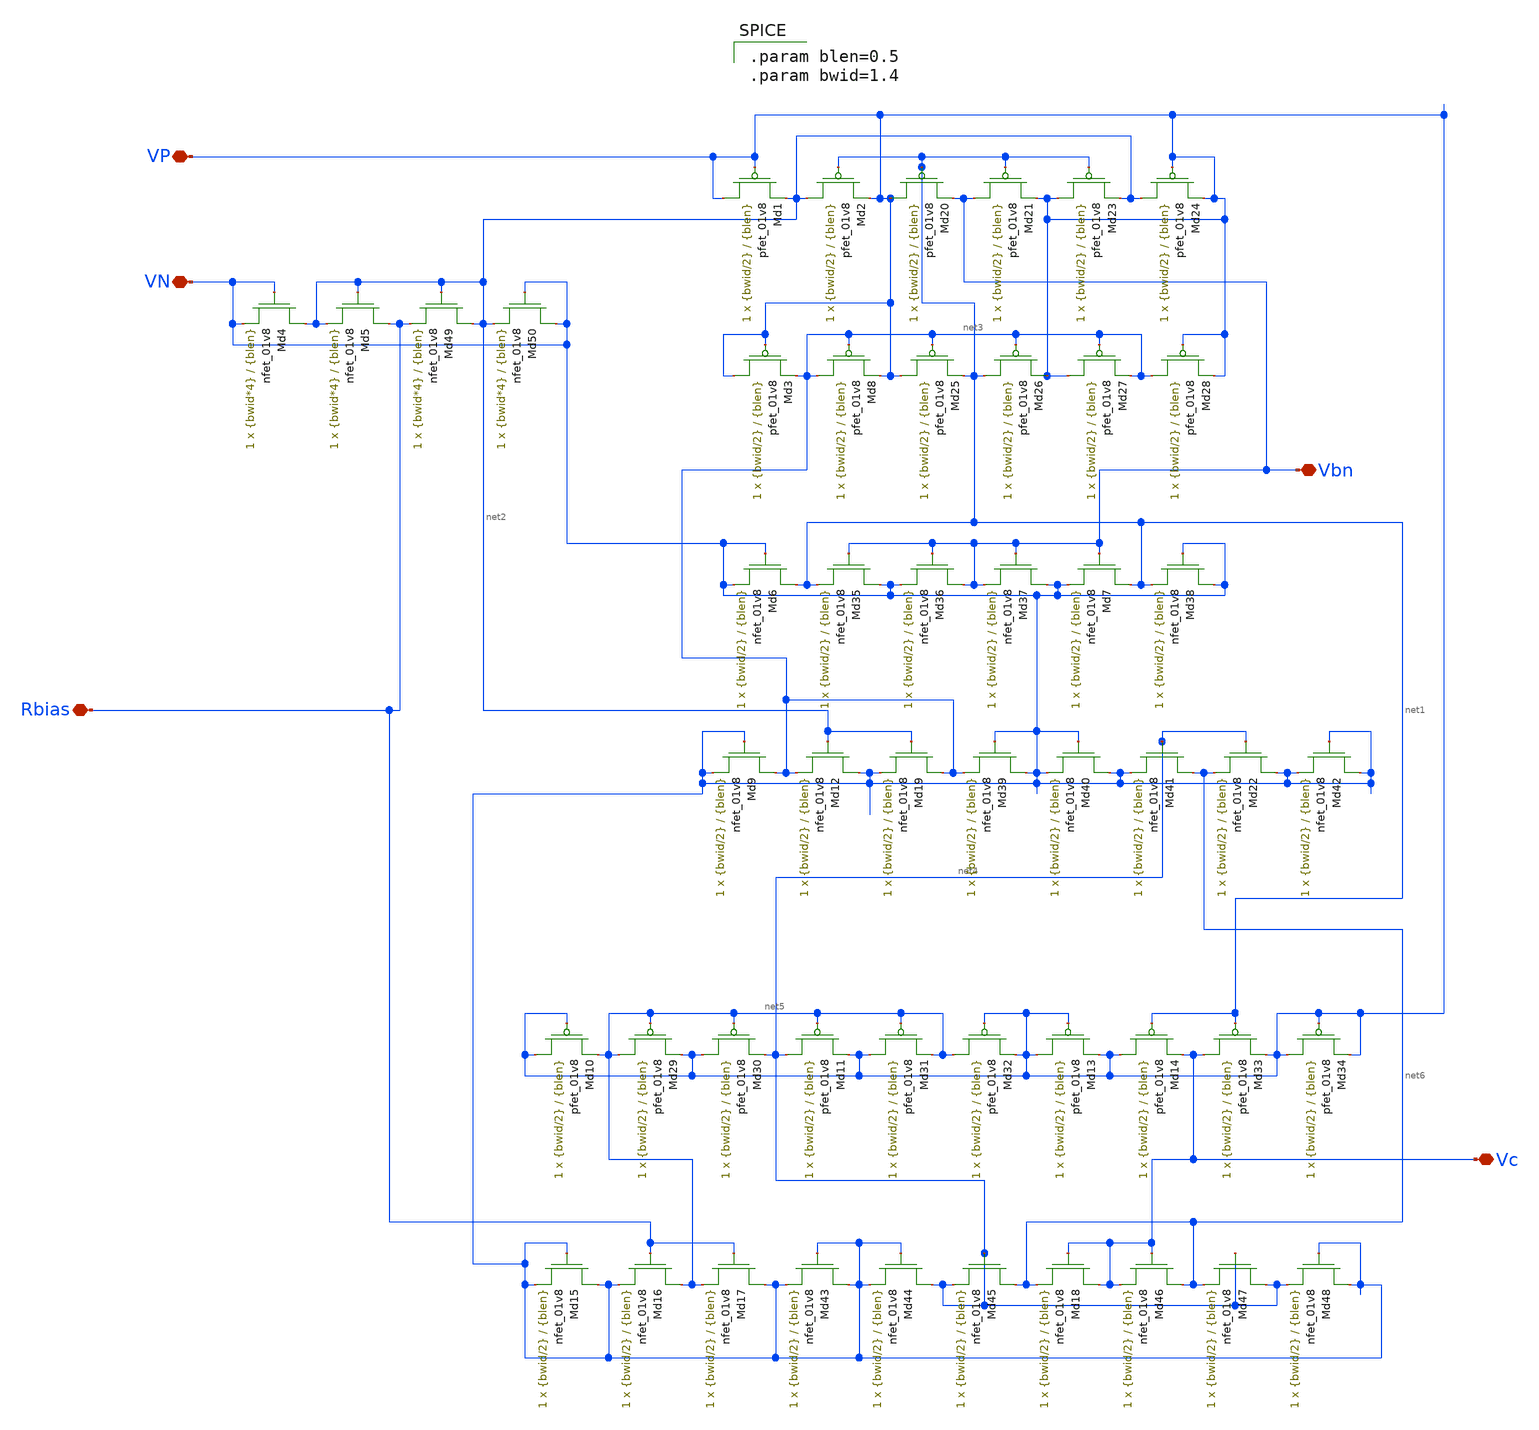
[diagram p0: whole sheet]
** sch_path: design-files/opt/biasgen_opt.sch
**.subckt biasgen_opt Rbias Vbn Vc VP VN
*.iopin Rbias
*.iopin Vbn
*.iopin Vc
*.iopin VP
*.iopin VN
XMd1 VP VP net2 VDD sky130_fd_pr__pfet_01v8 L={blen} W={bwid/2} nf=1 ad='int((nf+1)/2) * W/nf * 0.29'
+ as='int((nf+2)/2) * W/nf * 0.29' pd='2*int((nf+1)/2) * (W/nf + 0.29)' ps='2*int((nf+2)/2) * (W/nf + 0.29)'
+ nrd='0.29 / W' nrs='0.29 / W' sa=0 sb=0 sd=0 mult=1 m=1
XMd6 net1 VN VN GND sky130_fd_pr__nfet_01v8 L={blen} W={bwid/2} nf=1 ad='int((nf+1)/2) * W/nf * 0.29'
+ as='int((nf+2)/2) * W/nf * 0.29' pd='2*int((nf+1)/2) * (W/nf + 0.29)' ps='2*int((nf+2)/2) * (W/nf + 0.29)'
+ nrd='0.29 / W' nrs='0.29 / W' sa=0 sb=0 sd=0 mult=1 m=1
XMd2 net2 net1 VP VDD sky130_fd_pr__pfet_01v8 L={blen} W={bwid/2} nf=1 ad='int((nf+1)/2) * W/nf * 0.29'
+ as='int((nf+2)/2) * W/nf * 0.29' pd='2*int((nf+1)/2) * (W/nf + 0.29)' ps='2*int((nf+2)/2) * (W/nf + 0.29)'
+ nrd='0.29 / W' nrs='0.29 / W' sa=0 sb=0 sd=0 mult=1 m=1
XMd20 VP net1 Vbn VDD sky130_fd_pr__pfet_01v8 L={blen} W={bwid/2} nf=1 ad='int((nf+1)/2) * W/nf * 0.29'
+ as='int((nf+2)/2) * W/nf * 0.29' pd='2*int((nf+1)/2) * (W/nf + 0.29)' ps='2*int((nf+2)/2) * (W/nf + 0.29)'
+ nrd='0.29 / W' nrs='0.29 / W' sa=0 sb=0 sd=0 mult=1 m=1
XMd21 Vbn net1 VP VDD sky130_fd_pr__pfet_01v8 L={blen} W={bwid/2} nf=1 ad='int((nf+1)/2) * W/nf * 0.29'
+ as='int((nf+2)/2) * W/nf * 0.29' pd='2*int((nf+1)/2) * (W/nf + 0.29)' ps='2*int((nf+2)/2) * (W/nf + 0.29)'
+ nrd='0.29 / W' nrs='0.29 / W' sa=0 sb=0 sd=0 mult=1 m=1
XMd23 VP net1 net2 VDD sky130_fd_pr__pfet_01v8 L={blen} W={bwid/2} nf=1 ad='int((nf+1)/2) * W/nf * 0.29'
+ as='int((nf+2)/2) * W/nf * 0.29' pd='2*int((nf+1)/2) * (W/nf + 0.29)' ps='2*int((nf+2)/2) * (W/nf + 0.29)'
+ nrd='0.29 / W' nrs='0.29 / W' sa=0 sb=0 sd=0 mult=1 m=1
XMd24 net2 VP VP VDD sky130_fd_pr__pfet_01v8 L={blen} W={bwid/2} nf=1 ad='int((nf+1)/2) * W/nf * 0.29'
+ as='int((nf+2)/2) * W/nf * 0.29' pd='2*int((nf+1)/2) * (W/nf + 0.29)' ps='2*int((nf+2)/2) * (W/nf + 0.29)'
+ nrd='0.29 / W' nrs='0.29 / W' sa=0 sb=0 sd=0 mult=1 m=1
XMd3 VP VP net3 VDD sky130_fd_pr__pfet_01v8 L={blen} W={bwid/2} nf=1 ad='int((nf+1)/2) * W/nf * 0.29'
+ as='int((nf+2)/2) * W/nf * 0.29' pd='2*int((nf+1)/2) * (W/nf + 0.29)' ps='2*int((nf+2)/2) * (W/nf + 0.29)'
+ nrd='0.29 / W' nrs='0.29 / W' sa=0 sb=0 sd=0 mult=1 m=1
XMd8 net3 net3 VP VDD sky130_fd_pr__pfet_01v8 L={blen} W={bwid/2} nf=1 ad='int((nf+1)/2) * W/nf * 0.29'
+ as='int((nf+2)/2) * W/nf * 0.29' pd='2*int((nf+1)/2) * (W/nf + 0.29)' ps='2*int((nf+2)/2) * (W/nf + 0.29)'
+ nrd='0.29 / W' nrs='0.29 / W' sa=0 sb=0 sd=0 mult=1 m=1
XMd25 VP net3 net1 VDD sky130_fd_pr__pfet_01v8 L={blen} W={bwid/2} nf=1 ad='int((nf+1)/2) * W/nf * 0.29'
+ as='int((nf+2)/2) * W/nf * 0.29' pd='2*int((nf+1)/2) * (W/nf + 0.29)' ps='2*int((nf+2)/2) * (W/nf + 0.29)'
+ nrd='0.29 / W' nrs='0.29 / W' sa=0 sb=0 sd=0 mult=1 m=1
XMd26 net1 net3 VP VDD sky130_fd_pr__pfet_01v8 L={blen} W={bwid/2} nf=1 ad='int((nf+1)/2) * W/nf * 0.29'
+ as='int((nf+2)/2) * W/nf * 0.29' pd='2*int((nf+1)/2) * (W/nf + 0.29)' ps='2*int((nf+2)/2) * (W/nf + 0.29)'
+ nrd='0.29 / W' nrs='0.29 / W' sa=0 sb=0 sd=0 mult=1 m=1
XMd27 VP net3 net3 VDD sky130_fd_pr__pfet_01v8 L={blen} W={bwid/2} nf=1 ad='int((nf+1)/2) * W/nf * 0.29'
+ as='int((nf+2)/2) * W/nf * 0.29' pd='2*int((nf+1)/2) * (W/nf + 0.29)' ps='2*int((nf+2)/2) * (W/nf + 0.29)'
+ nrd='0.29 / W' nrs='0.29 / W' sa=0 sb=0 sd=0 mult=1 m=1
XMd28 net3 VP VP VDD sky130_fd_pr__pfet_01v8 L={blen} W={bwid/2} nf=1 ad='int((nf+1)/2) * W/nf * 0.29'
+ as='int((nf+2)/2) * W/nf * 0.29' pd='2*int((nf+1)/2) * (W/nf + 0.29)' ps='2*int((nf+2)/2) * (W/nf + 0.29)'
+ nrd='0.29 / W' nrs='0.29 / W' sa=0 sb=0 sd=0 mult=1 m=1
XMd10 VP VP net5 VDD sky130_fd_pr__pfet_01v8 L={blen} W={bwid/2} nf=1 ad='int((nf+1)/2) * W/nf * 0.29'
+ as='int((nf+2)/2) * W/nf * 0.29' pd='2*int((nf+1)/2) * (W/nf + 0.29)' ps='2*int((nf+2)/2) * (W/nf + 0.29)'
+ nrd='0.29 / W' nrs='0.29 / W' sa=0 sb=0 sd=0 mult=1 m=1
XMd29 net5 net5 VP VDD sky130_fd_pr__pfet_01v8 L={blen} W={bwid/2} nf=1 ad='int((nf+1)/2) * W/nf * 0.29'
+ as='int((nf+2)/2) * W/nf * 0.29' pd='2*int((nf+1)/2) * (W/nf + 0.29)' ps='2*int((nf+2)/2) * (W/nf + 0.29)'
+ nrd='0.29 / W' nrs='0.29 / W' sa=0 sb=0 sd=0 mult=1 m=1
XMd30 VP net5 net4 VDD sky130_fd_pr__pfet_01v8 L={blen} W={bwid/2} nf=1 ad='int((nf+1)/2) * W/nf * 0.29'
+ as='int((nf+2)/2) * W/nf * 0.29' pd='2*int((nf+1)/2) * (W/nf + 0.29)' ps='2*int((nf+2)/2) * (W/nf + 0.29)'
+ nrd='0.29 / W' nrs='0.29 / W' sa=0 sb=0 sd=0 mult=1 m=1
XMd11 net4 net5 VP VDD sky130_fd_pr__pfet_01v8 L={blen} W={bwid/2} nf=1 ad='int((nf+1)/2) * W/nf * 0.29'
+ as='int((nf+2)/2) * W/nf * 0.29' pd='2*int((nf+1)/2) * (W/nf + 0.29)' ps='2*int((nf+2)/2) * (W/nf + 0.29)'
+ nrd='0.29 / W' nrs='0.29 / W' sa=0 sb=0 sd=0 mult=1 m=1
XMd31 VP net5 net5 VDD sky130_fd_pr__pfet_01v8 L={blen} W={bwid/2} nf=1 ad='int((nf+1)/2) * W/nf * 0.29'
+ as='int((nf+2)/2) * W/nf * 0.29' pd='2*int((nf+1)/2) * (W/nf + 0.29)' ps='2*int((nf+2)/2) * (W/nf + 0.29)'
+ nrd='0.29 / W' nrs='0.29 / W' sa=0 sb=0 sd=0 mult=1 m=1
XMd32 net5 VP VP VDD sky130_fd_pr__pfet_01v8 L={blen} W={bwid/2} nf=1 ad='int((nf+1)/2) * W/nf * 0.29'
+ as='int((nf+2)/2) * W/nf * 0.29' pd='2*int((nf+1)/2) * (W/nf + 0.29)' ps='2*int((nf+2)/2) * (W/nf + 0.29)'
+ nrd='0.29 / W' nrs='0.29 / W' sa=0 sb=0 sd=0 mult=1 m=1
XMd13 VP VP VP VDD sky130_fd_pr__pfet_01v8 L={blen} W={bwid/2} nf=1 ad='int((nf+1)/2) * W/nf * 0.29'
+ as='int((nf+2)/2) * W/nf * 0.29' pd='2*int((nf+1)/2) * (W/nf + 0.29)' ps='2*int((nf+2)/2) * (W/nf + 0.29)'
+ nrd='0.29 / W' nrs='0.29 / W' sa=0 sb=0 sd=0 mult=1 m=1
XMd14 VP net1 Vc VDD sky130_fd_pr__pfet_01v8 L={blen} W={bwid/2} nf=1 ad='int((nf+1)/2) * W/nf * 0.29'
+ as='int((nf+2)/2) * W/nf * 0.29' pd='2*int((nf+1)/2) * (W/nf + 0.29)' ps='2*int((nf+2)/2) * (W/nf + 0.29)'
+ nrd='0.29 / W' nrs='0.29 / W' sa=0 sb=0 sd=0 mult=1 m=1
XMd33 Vc net1 VP VDD sky130_fd_pr__pfet_01v8 L={blen} W={bwid/2} nf=1 ad='int((nf+1)/2) * W/nf * 0.29'
+ as='int((nf+2)/2) * W/nf * 0.29' pd='2*int((nf+1)/2) * (W/nf + 0.29)' ps='2*int((nf+2)/2) * (W/nf + 0.29)'
+ nrd='0.29 / W' nrs='0.29 / W' sa=0 sb=0 sd=0 mult=1 m=1
XMd34 VP VP VP VDD sky130_fd_pr__pfet_01v8 L={blen} W={bwid/2} nf=1 ad='int((nf+1)/2) * W/nf * 0.29'
+ as='int((nf+2)/2) * W/nf * 0.29' pd='2*int((nf+1)/2) * (W/nf + 0.29)' ps='2*int((nf+2)/2) * (W/nf + 0.29)'
+ nrd='0.29 / W' nrs='0.29 / W' sa=0 sb=0 sd=0 mult=1 m=1
XMd35 VN Vbn net1 GND sky130_fd_pr__nfet_01v8 L={blen} W={bwid/2} nf=1 ad='int((nf+1)/2) * W/nf * 0.29'
+ as='int((nf+2)/2) * W/nf * 0.29' pd='2*int((nf+1)/2) * (W/nf + 0.29)' ps='2*int((nf+2)/2) * (W/nf + 0.29)'
+ nrd='0.29 / W' nrs='0.29 / W' sa=0 sb=0 sd=0 mult=1 m=1
XMd36 Vbn Vbn VN GND sky130_fd_pr__nfet_01v8 L={blen} W={bwid/2} nf=1 ad='int((nf+1)/2) * W/nf * 0.29'
+ as='int((nf+2)/2) * W/nf * 0.29' pd='2*int((nf+1)/2) * (W/nf + 0.29)' ps='2*int((nf+2)/2) * (W/nf + 0.29)'
+ nrd='0.29 / W' nrs='0.29 / W' sa=0 sb=0 sd=0 mult=1 m=1
XMd37 VN Vbn Vbn GND sky130_fd_pr__nfet_01v8 L={blen} W={bwid/2} nf=1 ad='int((nf+1)/2) * W/nf * 0.29'
+ as='int((nf+2)/2) * W/nf * 0.29' pd='2*int((nf+1)/2) * (W/nf + 0.29)' ps='2*int((nf+2)/2) * (W/nf + 0.29)'
+ nrd='0.29 / W' nrs='0.29 / W' sa=0 sb=0 sd=0 mult=1 m=1
XMd7 net1 Vbn VN GND sky130_fd_pr__nfet_01v8 L={blen} W={bwid/2} nf=1 ad='int((nf+1)/2) * W/nf * 0.29'
+ as='int((nf+2)/2) * W/nf * 0.29' pd='2*int((nf+1)/2) * (W/nf + 0.29)' ps='2*int((nf+2)/2) * (W/nf + 0.29)'
+ nrd='0.29 / W' nrs='0.29 / W' sa=0 sb=0 sd=0 mult=1 m=1
XMd38 VN VN net1 GND sky130_fd_pr__nfet_01v8 L={blen} W={bwid/2} nf=1 ad='int((nf+1)/2) * W/nf * 0.29'
+ as='int((nf+2)/2) * W/nf * 0.29' pd='2*int((nf+1)/2) * (W/nf + 0.29)' ps='2*int((nf+2)/2) * (W/nf + 0.29)'
+ nrd='0.29 / W' nrs='0.29 / W' sa=0 sb=0 sd=0 mult=1 m=1
XMd9 net3 VN VN GND sky130_fd_pr__nfet_01v8 L={blen} W={bwid/2} nf=1 ad='int((nf+1)/2) * W/nf * 0.29'
+ as='int((nf+2)/2) * W/nf * 0.29' pd='2*int((nf+1)/2) * (W/nf + 0.29)' ps='2*int((nf+2)/2) * (W/nf + 0.29)'
+ nrd='0.29 / W' nrs='0.29 / W' sa=0 sb=0 sd=0 mult=1 m=1
XMd12 VN net2 net3 GND sky130_fd_pr__nfet_01v8 L={blen} W={bwid/2} nf=1 ad='int((nf+1)/2) * W/nf * 0.29'
+ as='int((nf+2)/2) * W/nf * 0.29' pd='2*int((nf+1)/2) * (W/nf + 0.29)' ps='2*int((nf+2)/2) * (W/nf + 0.29)'
+ nrd='0.29 / W' nrs='0.29 / W' sa=0 sb=0 sd=0 mult=1 m=1
XMd19 net3 net2 VN GND sky130_fd_pr__nfet_01v8 L={blen} W={bwid/2} nf=1 ad='int((nf+1)/2) * W/nf * 0.29'
+ as='int((nf+2)/2) * W/nf * 0.29' pd='2*int((nf+1)/2) * (W/nf + 0.29)' ps='2*int((nf+2)/2) * (W/nf + 0.29)'
+ nrd='0.29 / W' nrs='0.29 / W' sa=0 sb=0 sd=0 mult=1 m=1
XMd39 VN VN net3 GND sky130_fd_pr__nfet_01v8 L={blen} W={bwid/2} nf=1 ad='int((nf+1)/2) * W/nf * 0.29'
+ as='int((nf+2)/2) * W/nf * 0.29' pd='2*int((nf+1)/2) * (W/nf + 0.29)' ps='2*int((nf+2)/2) * (W/nf + 0.29)'
+ nrd='0.29 / W' nrs='0.29 / W' sa=0 sb=0 sd=0 mult=1 m=1
XMd40 VN VN VN GND sky130_fd_pr__nfet_01v8 L={blen} W={bwid/2} nf=1 ad='int((nf+1)/2) * W/nf * 0.29'
+ as='int((nf+2)/2) * W/nf * 0.29' pd='2*int((nf+1)/2) * (W/nf + 0.29)' ps='2*int((nf+2)/2) * (W/nf + 0.29)'
+ nrd='0.29 / W' nrs='0.29 / W' sa=0 sb=0 sd=0 mult=1 m=1
XMd41 net6 net4 VN GND sky130_fd_pr__nfet_01v8 L={blen} W={bwid/2} nf=1 ad='int((nf+1)/2) * W/nf * 0.29'
+ as='int((nf+2)/2) * W/nf * 0.29' pd='2*int((nf+1)/2) * (W/nf + 0.29)' ps='2*int((nf+2)/2) * (W/nf + 0.29)'
+ nrd='0.29 / W' nrs='0.29 / W' sa=0 sb=0 sd=0 mult=1 m=1
XMd22 VN net4 net6 GND sky130_fd_pr__nfet_01v8 L={blen} W={bwid/2} nf=1 ad='int((nf+1)/2) * W/nf * 0.29'
+ as='int((nf+2)/2) * W/nf * 0.29' pd='2*int((nf+1)/2) * (W/nf + 0.29)' ps='2*int((nf+2)/2) * (W/nf + 0.29)'
+ nrd='0.29 / W' nrs='0.29 / W' sa=0 sb=0 sd=0 mult=1 m=1
XMd42 VN VN VN GND sky130_fd_pr__nfet_01v8 L={blen} W={bwid/2} nf=1 ad='int((nf+1)/2) * W/nf * 0.29'
+ as='int((nf+2)/2) * W/nf * 0.29' pd='2*int((nf+1)/2) * (W/nf + 0.29)' ps='2*int((nf+2)/2) * (W/nf + 0.29)'
+ nrd='0.29 / W' nrs='0.29 / W' sa=0 sb=0 sd=0 mult=1 m=1
XMd15 VN VN VN GND sky130_fd_pr__nfet_01v8 L={blen} W={bwid/2} nf=1 ad='int((nf+1)/2) * W/nf * 0.29'
+ as='int((nf+2)/2) * W/nf * 0.29' pd='2*int((nf+1)/2) * (W/nf + 0.29)' ps='2*int((nf+2)/2) * (W/nf + 0.29)'
+ nrd='0.29 / W' nrs='0.29 / W' sa=0 sb=0 sd=0 mult=1 m=1
XMd16 net5 Rbias VN GND sky130_fd_pr__nfet_01v8 L={blen} W={bwid/2} nf=1 ad='int((nf+1)/2) * W/nf * 0.29'
+ as='int((nf+2)/2) * W/nf * 0.29' pd='2*int((nf+1)/2) * (W/nf + 0.29)' ps='2*int((nf+2)/2) * (W/nf + 0.29)'
+ nrd='0.29 / W' nrs='0.29 / W' sa=0 sb=0 sd=0 mult=1 m=1
XMd17 VN Rbias net5 GND sky130_fd_pr__nfet_01v8 L={blen} W={bwid/2} nf=1 ad='int((nf+1)/2) * W/nf * 0.29'
+ as='int((nf+2)/2) * W/nf * 0.29' pd='2*int((nf+1)/2) * (W/nf + 0.29)' ps='2*int((nf+2)/2) * (W/nf + 0.29)'
+ nrd='0.29 / W' nrs='0.29 / W' sa=0 sb=0 sd=0 mult=1 m=1
XMd43 VN VN VN GND sky130_fd_pr__nfet_01v8 L={blen} W={bwid/2} nf=1 ad='int((nf+1)/2) * W/nf * 0.29'
+ as='int((nf+2)/2) * W/nf * 0.29' pd='2*int((nf+1)/2) * (W/nf + 0.29)' ps='2*int((nf+2)/2) * (W/nf + 0.29)'
+ nrd='0.29 / W' nrs='0.29 / W' sa=0 sb=0 sd=0 mult=1 m=1
XMd44 net4 VN VN GND sky130_fd_pr__nfet_01v8 L={blen} W={bwid/2} nf=1 ad='int((nf+1)/2) * W/nf * 0.29'
+ as='int((nf+2)/2) * W/nf * 0.29' pd='2*int((nf+1)/2) * (W/nf + 0.29)' ps='2*int((nf+2)/2) * (W/nf + 0.29)'
+ nrd='0.29 / W' nrs='0.29 / W' sa=0 sb=0 sd=0 mult=1 m=1
XMd45 net6 net4 net4 GND sky130_fd_pr__nfet_01v8 L={blen} W={bwid/2} nf=1 ad='int((nf+1)/2) * W/nf * 0.29'
+ as='int((nf+2)/2) * W/nf * 0.29' pd='2*int((nf+1)/2) * (W/nf + 0.29)' ps='2*int((nf+2)/2) * (W/nf + 0.29)'
+ nrd='0.29 / W' nrs='0.29 / W' sa=0 sb=0 sd=0 mult=1 m=1
XMd18 Vc Vc net6 GND sky130_fd_pr__nfet_01v8 L={blen} W={bwid/2} nf=1 ad='int((nf+1)/2) * W/nf * 0.29'
+ as='int((nf+2)/2) * W/nf * 0.29' pd='2*int((nf+1)/2) * (W/nf + 0.29)' ps='2*int((nf+2)/2) * (W/nf + 0.29)'
+ nrd='0.29 / W' nrs='0.29 / W' sa=0 sb=0 sd=0 mult=1 m=1
XMd46 net6 Vc Vc GND sky130_fd_pr__nfet_01v8 L={blen} W={bwid/2} nf=1 ad='int((nf+1)/2) * W/nf * 0.29'
+ as='int((nf+2)/2) * W/nf * 0.29' pd='2*int((nf+1)/2) * (W/nf + 0.29)' ps='2*int((nf+2)/2) * (W/nf + 0.29)'
+ nrd='0.29 / W' nrs='0.29 / W' sa=0 sb=0 sd=0 mult=1 m=1
XMd47 net4 net4 net6 GND sky130_fd_pr__nfet_01v8 L={blen} W={bwid/2} nf=1 ad='int((nf+1)/2) * W/nf * 0.29'
+ as='int((nf+2)/2) * W/nf * 0.29' pd='2*int((nf+1)/2) * (W/nf + 0.29)' ps='2*int((nf+2)/2) * (W/nf + 0.29)'
+ nrd='0.29 / W' nrs='0.29 / W' sa=0 sb=0 sd=0 mult=1 m=1
XMd48 VN VN net4 GND sky130_fd_pr__nfet_01v8 L={blen} W={bwid/2} nf=1 ad='int((nf+1)/2) * W/nf * 0.29'
+ as='int((nf+2)/2) * W/nf * 0.29' pd='2*int((nf+1)/2) * (W/nf + 0.29)' ps='2*int((nf+2)/2) * (W/nf + 0.29)'
+ nrd='0.29 / W' nrs='0.29 / W' sa=0 sb=0 sd=0 mult=1 m=1
XMd4 net2 VN VN GND sky130_fd_pr__nfet_01v8 L={blen} W={bwid*4} nf=1 ad='int((nf+1)/2) * W/nf * 0.29'
+ as='int((nf+2)/2) * W/nf * 0.29' pd='2*int((nf+1)/2) * (W/nf + 0.29)' ps='2*int((nf+2)/2) * (W/nf + 0.29)'
+ nrd='0.29 / W' nrs='0.29 / W' sa=0 sb=0 sd=0 mult=1 m=1
XMd5 Rbias net2 net2 GND sky130_fd_pr__nfet_01v8 L={blen} W={bwid*4} nf=1 ad='int((nf+1)/2) * W/nf * 0.29'
+ as='int((nf+2)/2) * W/nf * 0.29' pd='2*int((nf+1)/2) * (W/nf + 0.29)' ps='2*int((nf+2)/2) * (W/nf + 0.29)'
+ nrd='0.29 / W' nrs='0.29 / W' sa=0 sb=0 sd=0 mult=1 m=1
XMd49 net2 net2 Rbias GND sky130_fd_pr__nfet_01v8 L={blen} W={bwid*4} nf=1 ad='int((nf+1)/2) * W/nf * 0.29'
+ as='int((nf+2)/2) * W/nf * 0.29' pd='2*int((nf+1)/2) * (W/nf + 0.29)' ps='2*int((nf+2)/2) * (W/nf + 0.29)'
+ nrd='0.29 / W' nrs='0.29 / W' sa=0 sb=0 sd=0 mult=1 m=1
XMd50 VN VN net2 GND sky130_fd_pr__nfet_01v8 L={blen} W={bwid*4} nf=1 ad='int((nf+1)/2) * W/nf * 0.29'
+ as='int((nf+2)/2) * W/nf * 0.29' pd='2*int((nf+1)/2) * (W/nf + 0.29)' ps='2*int((nf+2)/2) * (W/nf + 0.29)'
+ nrd='0.29 / W' nrs='0.29 / W' sa=0 sb=0 sd=0 mult=1 m=1
**** begin user architecture code

.param blen=0.5
.param bwid=1.4

**** end user architecture code
**.ends
.end
